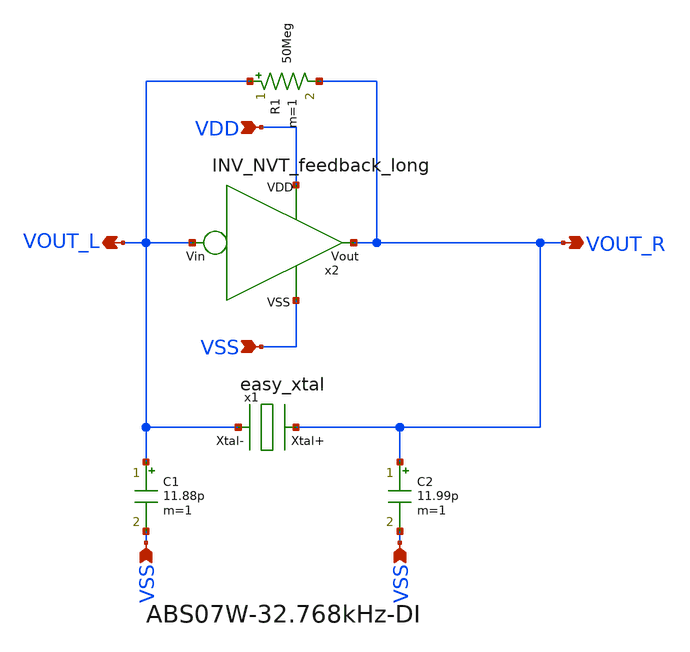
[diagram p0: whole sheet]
** sch_path: design/THESIS_EXP_RO_INVERTER_SKY130A/xtal_osc_NVT_L.sch
**.subckt xtal_osc_NVT_L VSS VSS VOUT_R VOUT_L VDD VSS
*.ipin VSS
*.ipin VSS
*.opin VOUT_R
*.opin VOUT_L
*.ipin VDD
*.ipin VSS
C1 VOUT_L VSS 11.88p m=1
C2 VOUT_R VSS 11.99p m=1
R1 VOUT_L VOUT_R 50Meg m=1
x2 VDD VSS VOUT_R VOUT_L INV_NVT_feedback_long
x1 VOUT_R VOUT_L easy_xtal
**.ends

* expanding   symbol:  THESIS_EXP_RO_INVERTER_SKY130A/INV_NVT_feedback_long.sym # of pins=4
** sym_path: design/THESIS_EXP_RO_INVERTER_SKY130A/INV_NVT_feedback_long.sym
** sch_path: design/THESIS_EXP_RO_INVERTER_SKY130A/INV_NVT_feedback_long.sch
.subckt INV_NVT_feedback_long VDD VSS Vout Vin
*.ipin VSS
*.ipin Vin
*.opin Vout
*.ipin VDD
XM1 Vout Vin VDD VDD sky130_fd_pr__pfet_01v8_lvt L=0.35 W=7 nf=1 ad='int((nf+1)/2) * W/nf * 0.29' as='int((nf+2)/2) * W/nf * 0.29'
+ pd='2*int((nf+1)/2) * (W/nf + 0.29)' ps='2*int((nf+2)/2) * (W/nf + 0.29)' nrd='0.29 / W' nrs='0.29 / W'
+ sa=0 sb=0 sd=0 mult=m_alpha m=m_alpha
XM2 Vout Vin vn VSS sky130_fd_pr__nfet_03v3_nvt L=0.8 W=0.42 nf=1 ad='int((nf+1)/2) * W/nf * 0.29' as='int((nf+2)/2) * W/nf * 0.29'
+ pd='2*int((nf+1)/2) * (W/nf + 0.29)' ps='2*int((nf+2)/2) * (W/nf + 0.29)' nrd='0.29 / W' nrs='0.29 / W'
+ sa=0 sb=0 sd=0 mult=m_beta m=m_beta
XM3 vn Vin VSS VSS sky130_fd_pr__nfet_03v3_nvt L=0.8 W=0.42 nf=1 ad='int((nf+1)/2) * W/nf * 0.29' as='int((nf+2)/2) * W/nf * 0.29'
+ pd='2*int((nf+1)/2) * (W/nf + 0.29)' ps='2*int((nf+2)/2) * (W/nf + 0.29)' nrd='0.29 / W' nrs='0.29 / W'
+ sa=0 sb=0 sd=0 mult=m_I0 m=m_I0
XM4 VDD Vout vn VSS sky130_fd_pr__nfet_03v3_nvt L=0.8 W=0.42 nf=1 ad='int((nf+1)/2) * W/nf * 0.29' as='int((nf+2)/2) * W/nf * 0.29'
+ pd='2*int((nf+1)/2) * (W/nf + 0.29)' ps='2*int((nf+2)/2) * (W/nf + 0.29)' nrd='0.29 / W' nrs='0.29 / W'
+ sa=0 sb=0 sd=0 mult=m_gamma m=m_gamma
.ends


* expanding   symbol:  THESIS_EXP_RO_INVERTER_SKY130A/easy_xtal.sym # of pins=2
** sym_path: design/THESIS_EXP_RO_INVERTER_SKY130A/easy_xtal.sym
** sch_path: design/THESIS_EXP_RO_INVERTER_SKY130A/easy_xtal.sch
.subckt easy_xtal Xtal+ Xtal-
*.iopin Xtal+
*.iopin Xtal-
R1 Xtal+ net1 30k m=1
C1 net1 net2 7.4f m=1
L1 net2 Xtal- 3187 m=1
C2 Xtal+ Xtal- 1p m=1
.ends

.end
